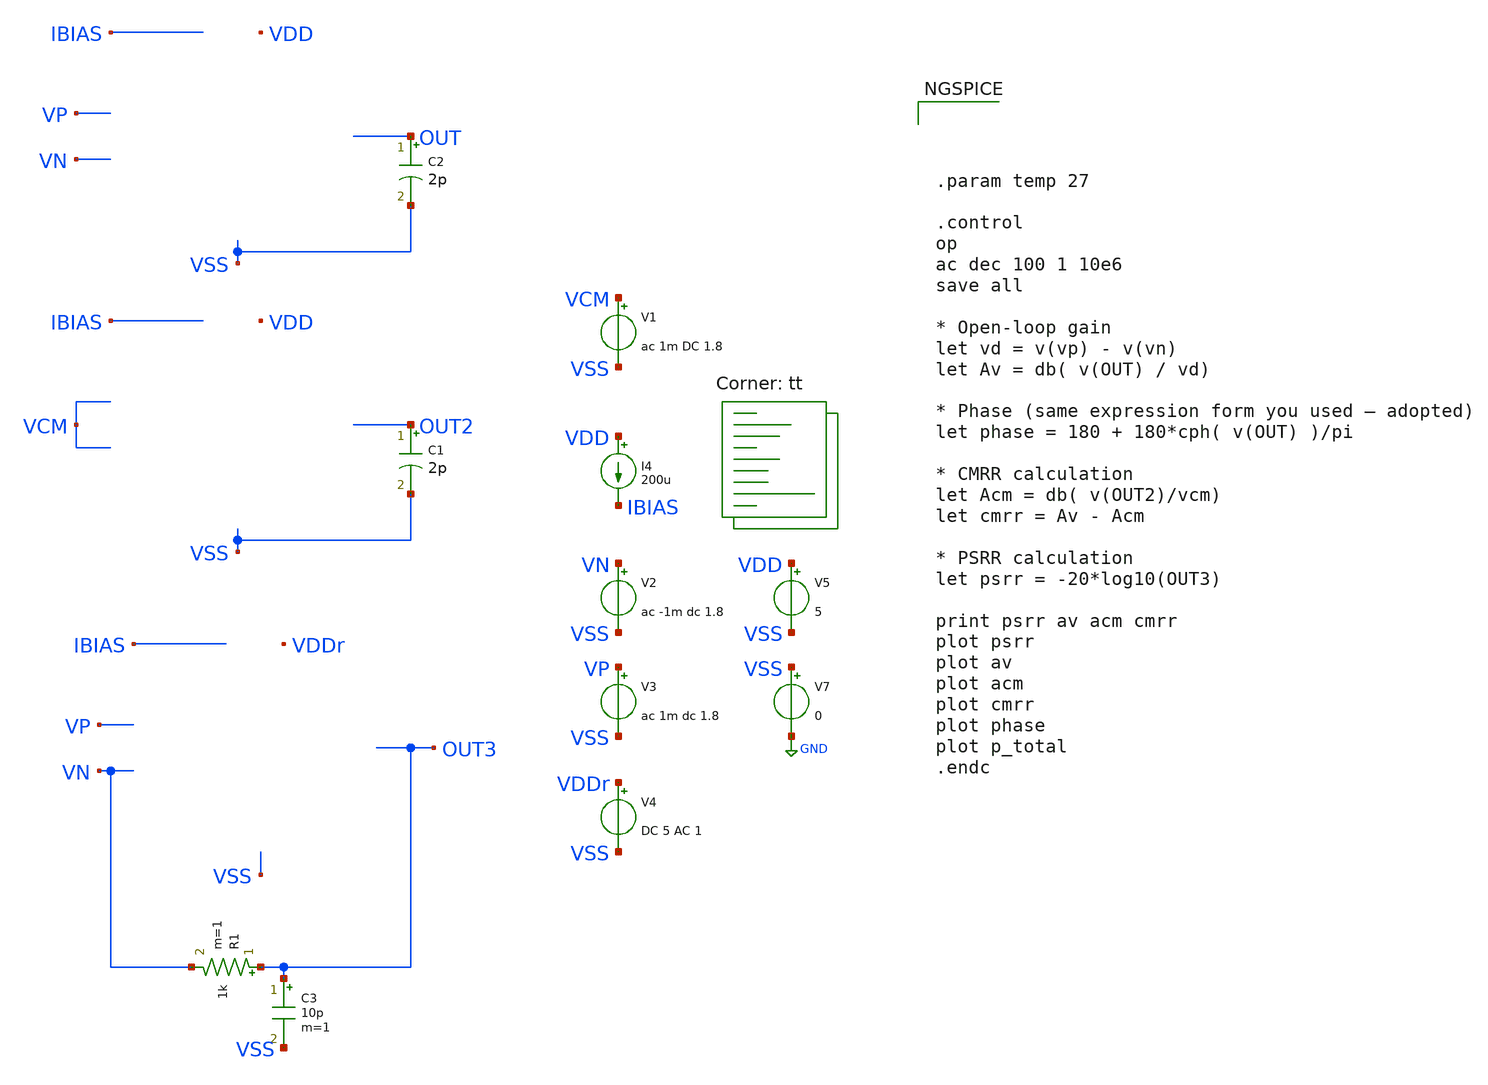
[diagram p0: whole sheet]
** sch_path: xschem/error-amplifier/testbench/untitled.sch
**.subckt untitled
V2 VN VSS ac -1m dc 1.8
V3 VP VSS ac 1m dc 1.8
V5 VDD VSS 5
V7 VSS GND 0
C2 OUT VSS 2p m=1
I4 VDD IBIAS 200u
C1 OUT2 VSS 2p m=1
V1 VCM VSS ac 1m DC 1.8
C3 OUT3 VSS 10p m=1
R1 OUT3 VN 1k m=1
V4 VDDr VSS DC 5 AC 1
**** begin user architecture code




.param temp 27

.control
op
ac dec 100 1 10e6
save all

* Open-loop gain
let vd = v(vp) - v(vn)
let Av = db( v(OUT) / vd)

* Phase (same expression form you used — adopted)
let phase = 180 + 180*cph( v(OUT) )/pi

* CMRR calculation
let Acm = db( v(OUT2)/vcm)
let cmrr = Av - Acm

* PSRR calculation
let psrr = -20*log10(OUT3)

print psrr av acm cmrr
plot psrr
plot av
plot acm
plot cmrr
plot phase
plot p_total
.endc



.lib $::SKYWATER_MODELS/sky130.lib.spice tt
**** end user architecture code
**.ends
.GLOBAL GND
.end
